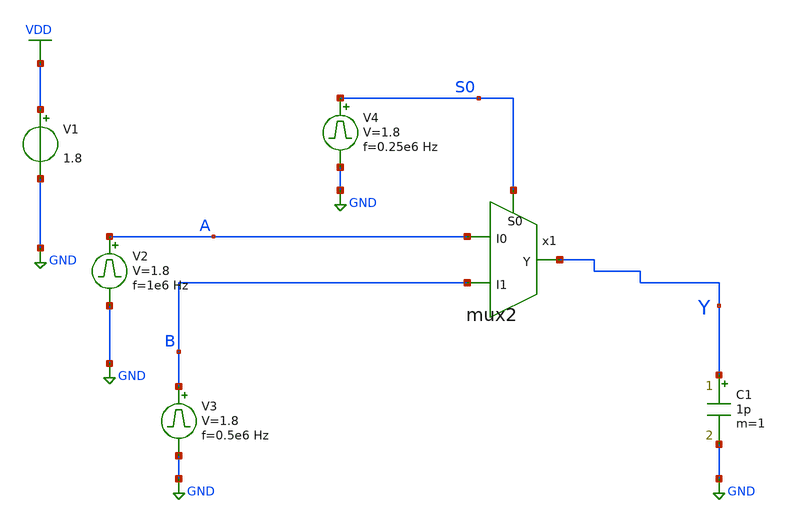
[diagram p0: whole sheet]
** sch_path: xschem/mux2_tb.sch
**.subckt mux2_tb
V1 VDD GND 1.8
V2 A GND pulse 0 1.8 '0.495/ 1e6 ' '0.01/1e6 ' '0.01/1e6 ' '0.49/1e6 ' '1/1e6 '
C1 Y GND 1p m=1
V3 B GND pulse 0 1.8 '0.495/ 0.5e6 ' '0.01/0.5e6 ' '0.01/0.5e6 ' '0.49/0.5e6 ' '1/0.5e6 '
V4 S0 GND pulse 0 1.8 '0.495/ 0.25e6 ' '0.01/0.25e6 ' '0.01/0.25e6 ' '0.49/0.25e6 ' '1/0.25e6 '
x1 B A S0 Y mux2
**** begin user architecture code


.control
save all
tran 1n 8u
plot V(A) V(B)+2 V(S0)+4 V(Y)+6
.endc



** opencircuitdesign pdks install
.lib $::SKYWATER_MODELS/sky130.lib.spice tt


**** end user architecture code
**.ends

* expanding   symbol:  mux2.sym # of pins=4
** sym_path: xschem/mux2.sym
** sch_path: xschem/mux2.sch
.subckt mux2 I1 I0 S0 Y
*.ipin I1
*.ipin I0
*.ipin S0
*.opin Y
XM9 net1 S0 I0 VDD sky130_fd_pr__pfet_01v8 L=0.15 W=1 nf=1 ad='int((nf+1)/2) * W/nf * 0.29' as='int((nf+2)/2) * W/nf * 0.29'
+ pd='2*int((nf+1)/2) * (W/nf + 0.29)' ps='2*int((nf+2)/2) * (W/nf + 0.29)' nrd='0.29 / W' nrs='0.29 / W'
+ sa=0 sb=0 sd=0 mult=1 m=1
XM10 net1 S0 I1 GND sky130_fd_pr__nfet_01v8 L=0.15 W=0.5 nf=1 ad='int((nf+1)/2) * W/nf * 0.29' as='int((nf+2)/2) * W/nf * 0.29'
+ pd='2*int((nf+1)/2) * (W/nf + 0.29)' ps='2*int((nf+2)/2) * (W/nf + 0.29)' nrd='0.29 / W' nrs='0.29 / W'
+ sa=0 sb=0 sd=0 mult=1 m=1
XM11 net2 net1 VDD VDD sky130_fd_pr__pfet_01v8 L=0.15 W=1 nf=1 ad='int((nf+1)/2) * W/nf * 0.29' as='int((nf+2)/2) * W/nf * 0.29'
+ pd='2*int((nf+1)/2) * (W/nf + 0.29)' ps='2*int((nf+2)/2) * (W/nf + 0.29)' nrd='0.29 / W' nrs='0.29 / W'
+ sa=0 sb=0 sd=0 mult=1 m=1
XM12 Y net2 VDD VDD sky130_fd_pr__pfet_01v8 L=0.15 W=1 nf=1 ad='int((nf+1)/2) * W/nf * 0.29' as='int((nf+2)/2) * W/nf * 0.29'
+ pd='2*int((nf+1)/2) * (W/nf + 0.29)' ps='2*int((nf+2)/2) * (W/nf + 0.29)' nrd='0.29 / W' nrs='0.29 / W'
+ sa=0 sb=0 sd=0 mult=1 m=1
XM13 net2 net1 GND GND sky130_fd_pr__nfet_01v8 L=0.15 W=0.5 nf=1 ad='int((nf+1)/2) * W/nf * 0.29' as='int((nf+2)/2) * W/nf * 0.29'
+ pd='2*int((nf+1)/2) * (W/nf + 0.29)' ps='2*int((nf+2)/2) * (W/nf + 0.29)' nrd='0.29 / W' nrs='0.29 / W'
+ sa=0 sb=0 sd=0 mult=1 m=1
XM14 Y net2 GND GND sky130_fd_pr__nfet_01v8 L=0.15 W=0.5 nf=1 ad='int((nf+1)/2) * W/nf * 0.29' as='int((nf+2)/2) * W/nf * 0.29'
+ pd='2*int((nf+1)/2) * (W/nf + 0.29)' ps='2*int((nf+2)/2) * (W/nf + 0.29)' nrd='0.29 / W' nrs='0.29 / W'
+ sa=0 sb=0 sd=0 mult=1 m=1
.ends

.GLOBAL VDD
.GLOBAL GND
.end
